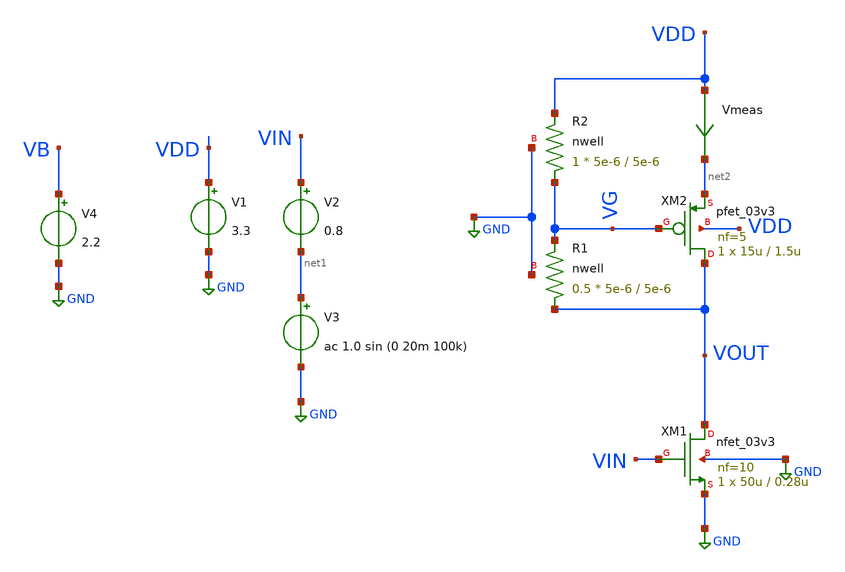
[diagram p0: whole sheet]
** sch_path: simple_amp9.sch
**.subckt simple_amp9
XM1 VOUT VIN GND GND nfet_03v3 L=0.28u W=50u nf=10 ad='int((nf+1)/2) * W/nf * 0.18u' as='int((nf+2)/2) * W/nf * 0.18u'
+ pd='2*int((nf+1)/2) * (W/nf + 0.18u)' ps='2*int((nf+2)/2) * (W/nf + 0.18u)' nrd='0.18u / W' nrs='0.18u / W'
+ sa=0 sb=0 sd=0 m=1
Vmeas VDD net2 0
.save i(vmeas)
V1 VDD GND 3.3
V2 VIN net1 0.8
XR2 VG VDD GND nwell r_width=5e-6 r_length=5e-6 m=1
V3 net1 GND ac 1.0 sin (0 20m 100k)
XM2 VOUT VG net2 VDD pfet_03v3 L=1.5u W=15u nf=5 ad='int((nf+1)/2) * W/nf * 0.18u' as='int((nf+2)/2) * W/nf * 0.18u'
+ pd='2*int((nf+1)/2) * (W/nf + 0.18u)' ps='2*int((nf+2)/2) * (W/nf + 0.18u)' nrd='0.18u / W' nrs='0.18u / W'
+ sa=0 sb=0 sd=0 m=1
V4 VB GND 2.2
XR1 VOUT VG GND nwell r_width=5e-6 r_length=5e-6 m=0.5
**** begin user architecture code

.include $::180MCU_MODELS/design.ngspice
*.lib $::180MCU_MODELS/sm141064.ngspice statistical
*.lib $::180MCU_MODELS/sm141064.ngspice res_statistical
.lib $::180MCU_MODELS/sm141064.ngspice typical
.lib $::180MCU_MODELS/sm141064.ngspice res_typical
.lib $::180MCU_MODELS/sm141064.ngspice moscap_typical
.lib $::180MCU_MODELS/sm141064.ngspice bjt_typical
.lib $::180MCU_MODELS/sm141064.ngspice diode_typical
.lib $::180MCU_MODELS/sm141064.ngspice mimcap_typical
.TEMP 27

.param   sw_stat_global = 1   sw_stat_mism = 1  mc_skew = 3  res_mc_skew = 3  cap_mc_skew = 3
+  fnoicor = 1



.control
save all
dc V2 0 3.3 0.01


plot v(VOUT) deriv(v(VOUT)) v(VIN)
plot deriv(v(VOUT)) (v(VDD)-v(VG)) (v(VDD)-v(VOUT))
plot i(Vmeas)
plot deriv(v(VOUT))
tran 10ns 20u
plot (v(VOUT)-1.27510) (v(VIN)-0.8)
plot fft((v(VOUT))) fft((v(VIN)))
ac dec 20 1 50G
plot v(VOUT)
.endc

**** end user architecture code
**.ends
.GLOBAL GND
.end
